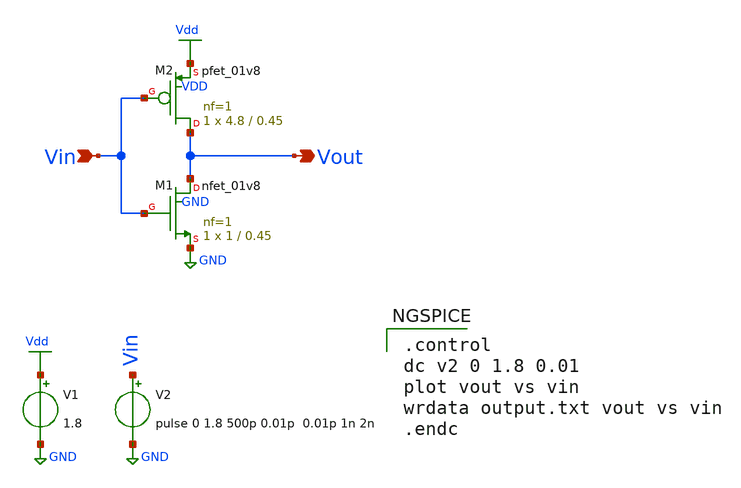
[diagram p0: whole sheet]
** sch_path: Circuiti/porta-not-caratteristica.sch
**.subckt porta-not-caratteristica Vin Vout
*.ipin Vin
*.opin Vout
XM1 Vout Vin GND GND sky130_fd_pr__nfet_01v8 L=0.45 W=1 nf=1 ad='int((nf+1)/2) * W/nf * 0.29' as='int((nf+2)/2) * W/nf * 0.29'
+ pd='2*int((nf+1)/2) * (W/nf + 0.29)' ps='2*int((nf+2)/2) * (W/nf + 0.29)' nrd='0.29 / W' nrs='0.29 / W'
+ sa=0 sb=0 sd=0 mult=1 m=1
V1 Vdd GND 1.8
XM2 Vout Vin Vdd VDD sky130_fd_pr__pfet_01v8 L=0.45 W=4.8 nf=1 ad='int((nf+1)/2) * W/nf * 0.29' as='int((nf+2)/2) * W/nf * 0.29'
+ pd='2*int((nf+1)/2) * (W/nf + 0.29)' ps='2*int((nf+2)/2) * (W/nf + 0.29)' nrd='0.29 / W' nrs='0.29 / W'
+ sa=0 sb=0 sd=0 mult=1 m=1
V2 Vin GND pulse 0 1.8 500p 0.01p 0.01p 1n 2n
**** begin user architecture code


.lib /home/matteo/xschem_downloads/skywater-pdk/libraries/sky130_fd_pr_ngspice/latest/models/sky130.lib.spice tt

*.include /home/matteo/xschem_downloads/skywater-pdk/libraries/sky130_fd_pr_ngspice/latest/cells/nfet_01v8/sky130_fd_pr__nfet_01v8__tt.corner.spice

.param mc_mm_switch=0
.param mc_pr_switch=1



.control
dc v2 0 1.8 0.01
plot vout vs vin
wrdata output.txt vout vs vin
.endc


**** end user architecture code
**.ends
.GLOBAL Vdd
.GLOBAL GND
.end
